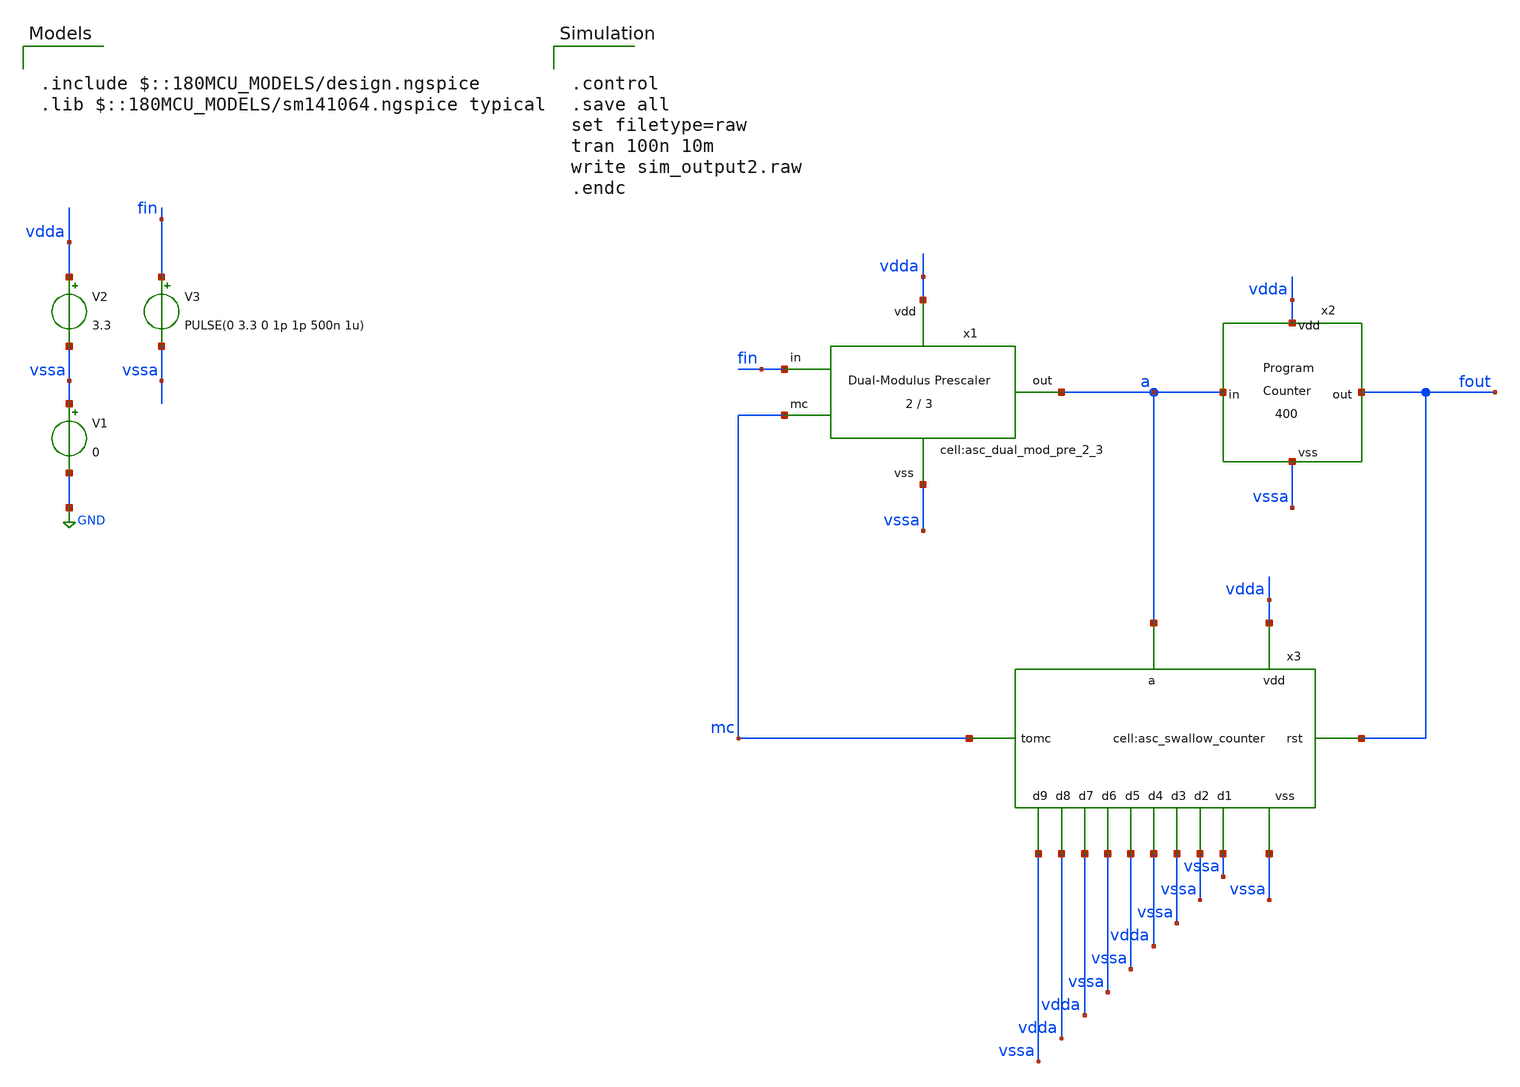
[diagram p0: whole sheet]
** sch_path: designs/libs/tb_analog/tb_pulse_swallow_divider/tb_pulse_swallow_divider.sch
**.subckt tb_pulse_swallow_divider
V1 vssa GND 0
V2 vdda vssa 3.3
V3 fin vssa PULSE(0 3.3 0 1p 1p 500n 1u)
x1 vdda vssa a fin mc asc_dual_mod_pre_2_3
x2 a fout vdda vssa asc_program_counter_400
x3 mc vssa vdda vdda vssa vssa vdda vssa vssa vssa vssa fout vdda a asc_swallow_counter
**** begin user architecture code

.include $::180MCU_MODELS/design.ngspice
.lib $::180MCU_MODELS/sm141064.ngspice typical



.control
.save all
set filetype=raw
tran 100n 10m
write sim_output2.raw
.endc


**** end user architecture code
**.ends
.GLOBAL GND
.end
